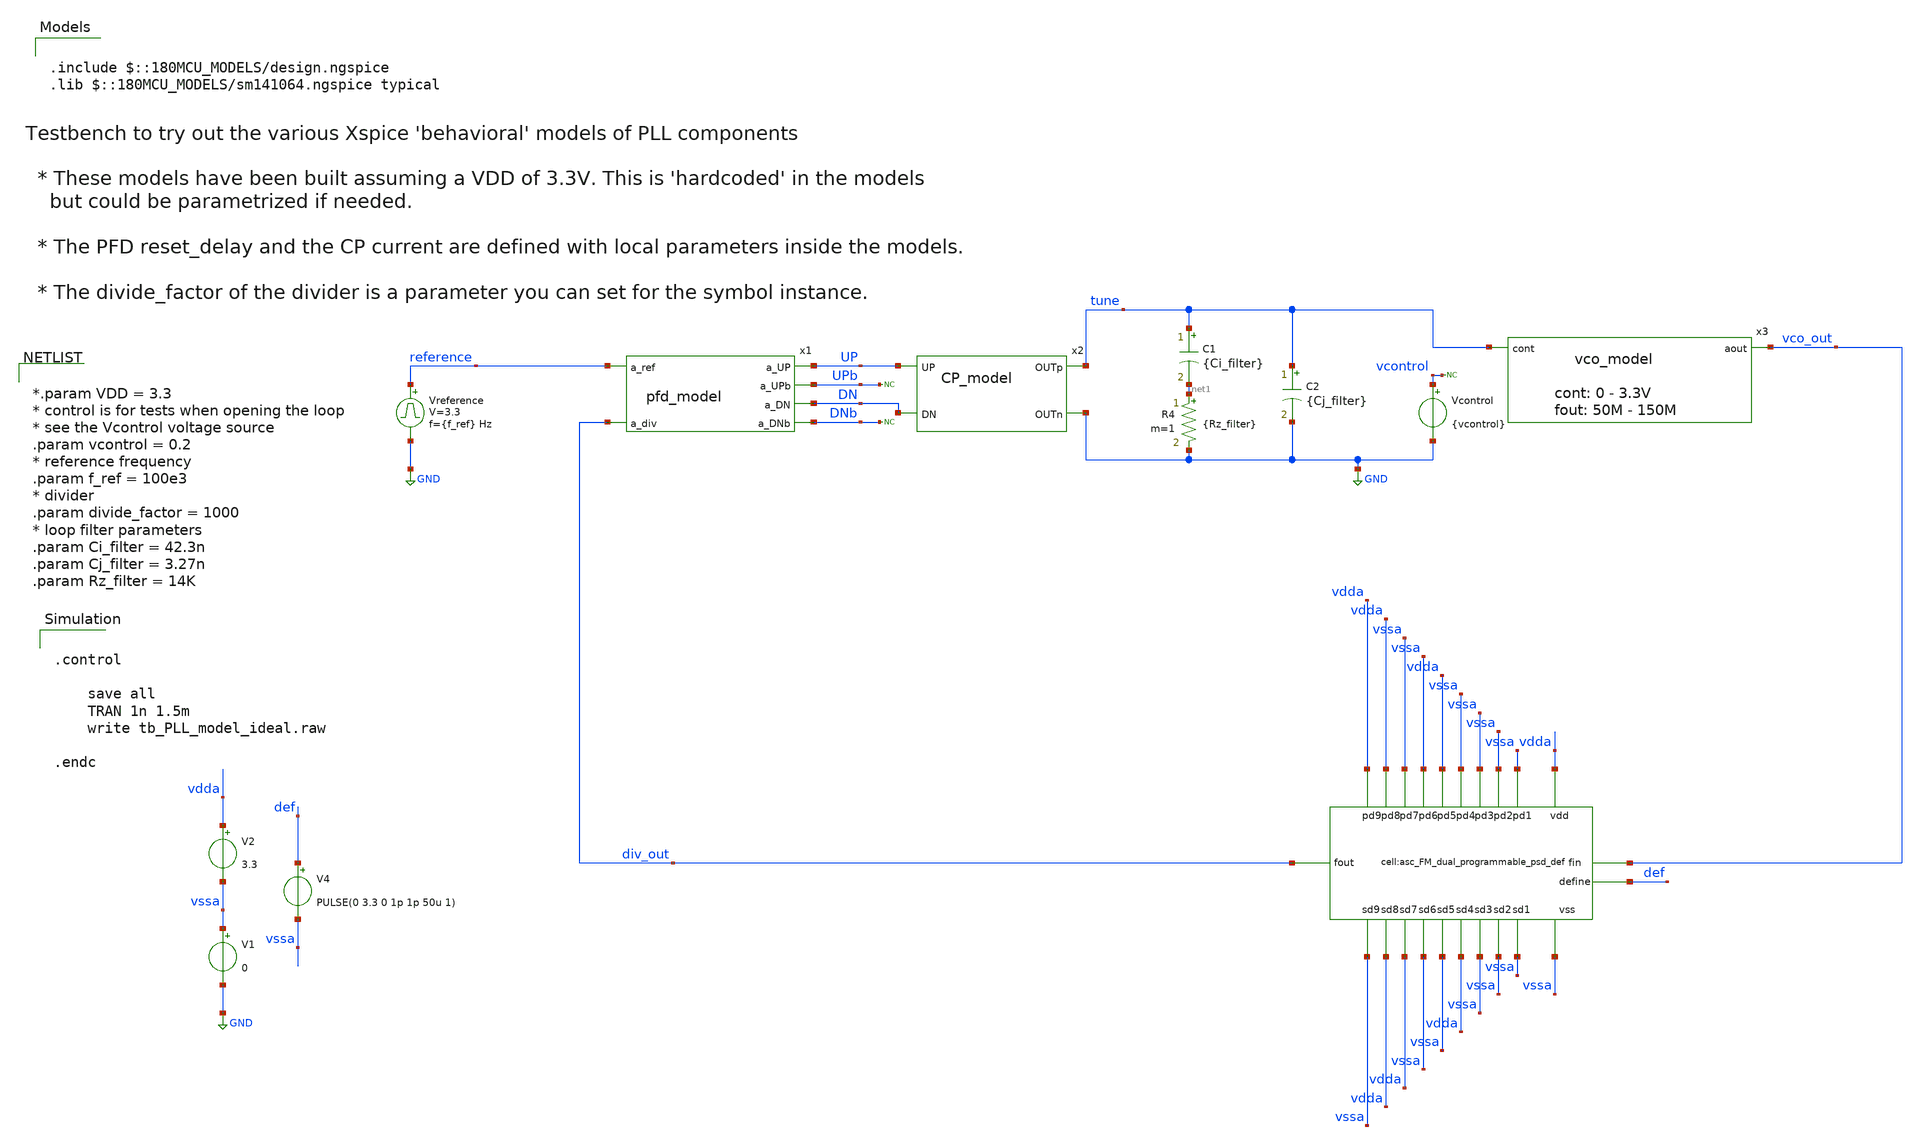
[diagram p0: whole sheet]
** sch_path: designs/libs/tb_pll/tb_PLL_PSD_model.sch
**.subckt tb_PLL_PSD_model
Vcontrol vcontrol GND {vcontrol}
Vreference reference GND pulse 0 3.3 '0.495/ {f_ref} ' '0.01/{f_ref} ' '0.01/{f_ref} ' '0.49/{f_ref} '
+ '1/{f_ref} '
C1 tune net1 {Ci_filter} m=1
R4 net1 GND {Rz_filter} m=1
* noconn vcontrol
* noconn UPb
* noconn DNb
C2 tune GND {Cj_filter} m=1
x1 reference UP UPb DN div_out DNb pfd_model
x2 tune UP DN GND CP_model
x3 vco_out tune vco_model
V1 vssa GND 0
V2 vdda vssa 3.3
V4 def vssa PULSE(0 3.3 0 1p 1p 50u 1)
**** begin user architecture code


.control

    save all
    TRAN 1n 1.5m
    write tb_PLL_model_ideal.raw

.endc




*.param VDD = 3.3
* control is for tests when opening the loop
* see the Vcontrol voltage source
.param vcontrol = 0.2
* reference frequency
.param f_ref = 100e3
* divider
.param divide_factor = 1000
* loop filter parameters
.param Ci_filter = 42.3n
.param Cj_filter = 3.27n
.param Rz_filter = 14K



.include $::180MCU_MODELS/design.ngspice
.lib $::180MCU_MODELS/sm141064.ngspice typical

**** end user architecture code
**.ends

* expanding   symbol:  libs/model_pll/pfd_model.sym # of pins=6
** sym_path: designs/libs/model_pll/pfd_model.sym
** sch_path: designs/libs/model_pll/pfd_model.sch
.subckt pfd_model a_ref a_UP a_UPb a_DN a_div a_DNb
*.ipin a_ref
*.ipin a_div
*.opin a_UP
*.opin a_UPb
*.opin a_DN
*.opin a_DNb
**** begin user architecture code



* PFD Model using digital Xspice components
*
* At the end we add the necessary a-d and d-a blocks so the
* signals can be put on pins or the internal signals can be
* observed when plotting (the latter is for debugging)

* pfd_delay local parameter sets the duration of the a_UP and a_DN
* signals; it is implemented with the reset_delay of
* the flip flops

.param pfd_delay = 10n

** Digital 1 and 0 to drive Flip-Flops
aone 0 d_d1 d_inv
azero d_d1 d_d0 d_inv
.model d_inv d_inverter()

** Flip Flops
ad1 d_d1 d_R d_d0 d_rset d_U d_U_ flop1
ad2 d_d1 d_V d_d0 d_rset d_D d_D_ flop1
.model flop1 d_dff(clk_delay = 1.0e-10 set_delay = 1.0e-10  reset_delay = {pfd_delay} ic = 2 rise_delay
+ = 1.0e-10  fall_delay = 1e-10)

* AND Gate
aa1 [d_U d_D] d_rset and1
.model and1 d_and(rise_delay = 1e-10 fall_delay = 1e-10  input_load = 0.5e-12)

aADC [ a_ref a_div ] [ d_R d_V ] adc_buff
.model adc_buff adc_bridge(in_low = 1.6 in_high = 1.7)

aDAC [ d_U d_U_ d_D d_D_ d_rset d_R d_V d_d1 d_d0 ] [ a_UP a_UPb a_DN a_DNb a_rset a_R a_V a_d1
+ a_d0] dac_buff
.model dac_buff dac_bridge(out_low = 0 out_high = 3.3)



**** end user architecture code
* noconn a_ref
* noconn a_div
* noconn a_UP
* noconn a_UPb
* noconn a_DN
* noconn a_DNb
.ends


* expanding   symbol:  libs/model_pll/CP_model.sym # of pins=4
** sym_path: designs/libs/model_pll/CP_model.sym
** sch_path: designs/libs/model_pll/CP_model.sch
.subckt CP_model OUTp UP DN OUTn
*.ipin UP
*.ipin DN
*.opin OUTp
*.opin OUTn
G1 OUTn OUTp UP DN {Gm_CP}
**** begin user architecture code


* Charge Pump Model
*

* local parameter Gm_CP sets the charge pump gain
* UP and DN are 0 or 3.3 so for an ICP of 1mA you
* need a Gm of 1m/3.3
*
*
* In single-ended applications, connect the OUTn to ground or VSS
* and the OUTp to the loop filter

.param ICP = 1m
.param VDD = 3.3
.param Gm_CP = {ICP/VDD}



**** end user architecture code
.ends


* expanding   symbol:  libs/model_pll/vco_model.sym # of pins=2
** sym_path: designs/libs/model_pll/vco_model.sym
** sch_path: designs/libs/model_pll/vco_model.sch
.subckt vco_model aout cont
*.ipin cont
*.opin aout
**** begin user architecture code


***** XSPICE analog sine VCO ***************
* 50 MHz to 150 MHz
* aout analog out
* cont control voltage between 0 and 3.3V
* KVCO = (150-50)/(3.3 - 0) MHz/V

asine cont aout analog_sin_osc
.model analog_sin_osc sine(cntl_array = [ 0    3.3 ]                           freq_array = [50e6
+ 150e6]                           out_high = 3.0 out_low = 0.3 )



**** end user architecture code
* noconn aout
* noconn cont
.ends

.GLOBAL GND
.end
